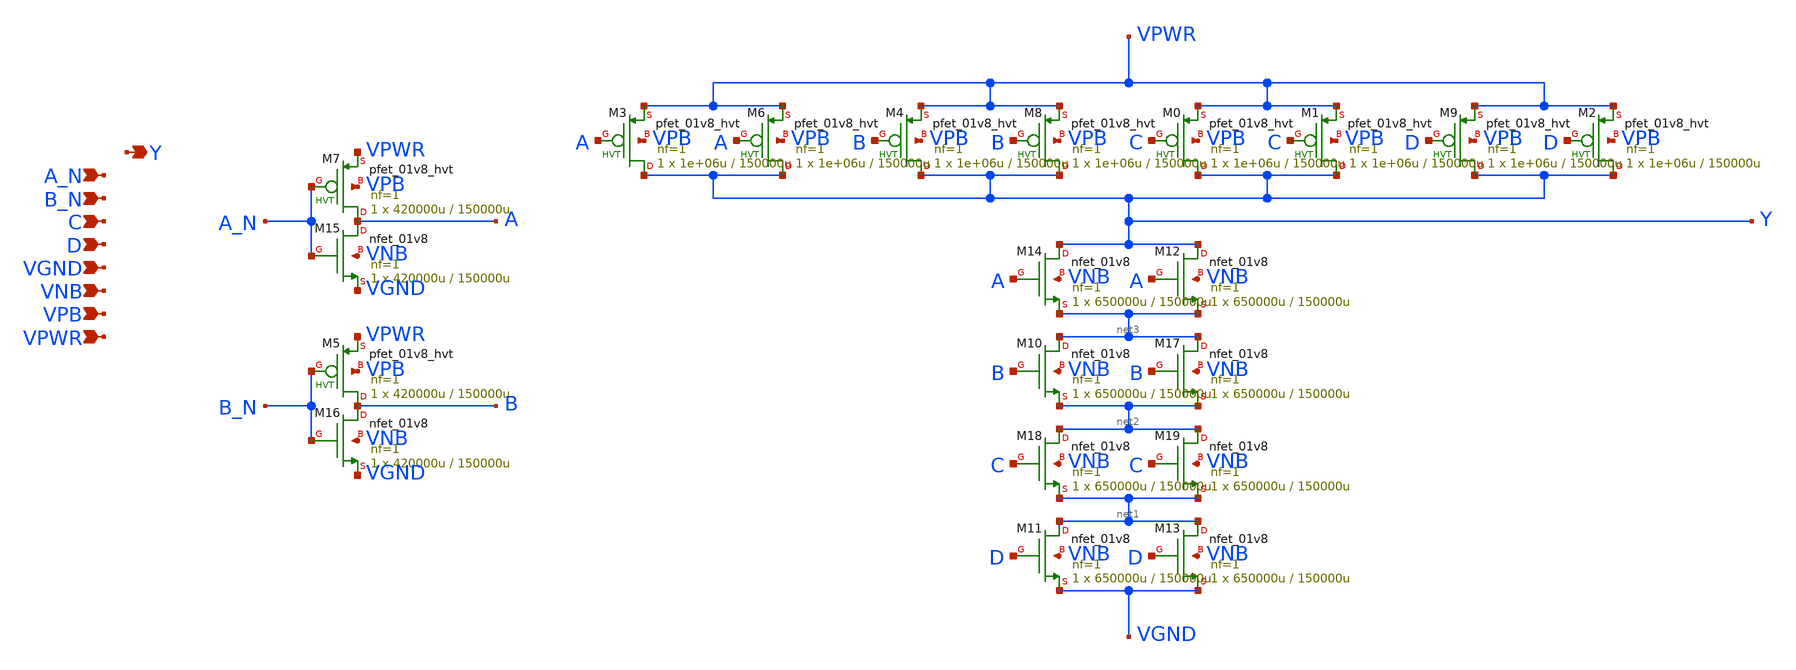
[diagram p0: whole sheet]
** sch_path: schematics/nand4bb/sky130_fd_sc_hd__nand4bb_2.sch
**.subckt sky130_fd_sc_hd__nand4bb_2 A_N B_N C D VGND VNB VPB VPWR Y
*.ipin A_N
*.ipin B_N
*.ipin C
*.ipin D
*.ipin VGND
*.ipin VNB
*.ipin VPB
*.ipin VPWR
*.opin Y
XM0 Y C VPWR VPB sky130_fd_pr__pfet_01v8_hvt L=150000u W=1e+06u nf=1 ad='int((1 + 1)/2) * 1e+06u / 1 * 0.29'
+ as='int((1 + 2)/2) * 1e+06u / 1 * 0.29' pd='2*int((1 + 1)/2) * (1e+06u / 1 + 0.29)' ps='2*int((1 + 2)/2) * (1e+06u / 1 + 0.29)'
+ nrd='0.29 / 1e+06u ' nrs='0.29 / 1e+06u ' sa=0 sb=0 sd=0 mult=1 m=1
XM1 Y C VPWR VPB sky130_fd_pr__pfet_01v8_hvt L=150000u W=1e+06u nf=1 ad='int((1 + 1)/2) * 1e+06u / 1 * 0.29'
+ as='int((1 + 2)/2) * 1e+06u / 1 * 0.29' pd='2*int((1 + 1)/2) * (1e+06u / 1 + 0.29)' ps='2*int((1 + 2)/2) * (1e+06u / 1 + 0.29)'
+ nrd='0.29 / 1e+06u ' nrs='0.29 / 1e+06u ' sa=0 sb=0 sd=0 mult=1 m=1
XM2 Y D VPWR VPB sky130_fd_pr__pfet_01v8_hvt L=150000u W=1e+06u nf=1 ad='int((1 + 1)/2) * 1e+06u / 1 * 0.29'
+ as='int((1 + 2)/2) * 1e+06u / 1 * 0.29' pd='2*int((1 + 1)/2) * (1e+06u / 1 + 0.29)' ps='2*int((1 + 2)/2) * (1e+06u / 1 + 0.29)'
+ nrd='0.29 / 1e+06u ' nrs='0.29 / 1e+06u ' sa=0 sb=0 sd=0 mult=1 m=1
XM3 Y A VPWR VPB sky130_fd_pr__pfet_01v8_hvt L=150000u W=1e+06u nf=1 ad='int((1 + 1)/2) * 1e+06u / 1 * 0.29'
+ as='int((1 + 2)/2) * 1e+06u / 1 * 0.29' pd='2*int((1 + 1)/2) * (1e+06u / 1 + 0.29)' ps='2*int((1 + 2)/2) * (1e+06u / 1 + 0.29)'
+ nrd='0.29 / 1e+06u ' nrs='0.29 / 1e+06u ' sa=0 sb=0 sd=0 mult=1 m=1
XM4 Y B VPWR VPB sky130_fd_pr__pfet_01v8_hvt L=150000u W=1e+06u nf=1 ad='int((1 + 1)/2) * 1e+06u / 1 * 0.29'
+ as='int((1 + 2)/2) * 1e+06u / 1 * 0.29' pd='2*int((1 + 1)/2) * (1e+06u / 1 + 0.29)' ps='2*int((1 + 2)/2) * (1e+06u / 1 + 0.29)'
+ nrd='0.29 / 1e+06u ' nrs='0.29 / 1e+06u ' sa=0 sb=0 sd=0 mult=1 m=1
XM5 B B_N VPWR VPB sky130_fd_pr__pfet_01v8_hvt L=150000u W=420000u nf=1 ad='int((1 + 1)/2) * 420000u / 1 * 0.29'
+ as='int((1 + 2)/2) * 420000u / 1 * 0.29' pd='2*int((1 + 1)/2) * (420000u / 1 + 0.29)' ps='2*int((1 + 2)/2) * (420000u / 1 + 0.29)'
+ nrd='0.29 / 420000u ' nrs='0.29 / 420000u ' sa=0 sb=0 sd=0 mult=1 m=1
XM6 Y A VPWR VPB sky130_fd_pr__pfet_01v8_hvt L=150000u W=1e+06u nf=1 ad='int((1 + 1)/2) * 1e+06u / 1 * 0.29'
+ as='int((1 + 2)/2) * 1e+06u / 1 * 0.29' pd='2*int((1 + 1)/2) * (1e+06u / 1 + 0.29)' ps='2*int((1 + 2)/2) * (1e+06u / 1 + 0.29)'
+ nrd='0.29 / 1e+06u ' nrs='0.29 / 1e+06u ' sa=0 sb=0 sd=0 mult=1 m=1
XM7 A A_N VPWR VPB sky130_fd_pr__pfet_01v8_hvt L=150000u W=420000u nf=1 ad='int((1 + 1)/2) * 420000u / 1 * 0.29'
+ as='int((1 + 2)/2) * 420000u / 1 * 0.29' pd='2*int((1 + 1)/2) * (420000u / 1 + 0.29)' ps='2*int((1 + 2)/2) * (420000u / 1 + 0.29)'
+ nrd='0.29 / 420000u ' nrs='0.29 / 420000u ' sa=0 sb=0 sd=0 mult=1 m=1
XM8 Y B VPWR VPB sky130_fd_pr__pfet_01v8_hvt L=150000u W=1e+06u nf=1 ad='int((1 + 1)/2) * 1e+06u / 1 * 0.29'
+ as='int((1 + 2)/2) * 1e+06u / 1 * 0.29' pd='2*int((1 + 1)/2) * (1e+06u / 1 + 0.29)' ps='2*int((1 + 2)/2) * (1e+06u / 1 + 0.29)'
+ nrd='0.29 / 1e+06u ' nrs='0.29 / 1e+06u ' sa=0 sb=0 sd=0 mult=1 m=1
XM9 Y D VPWR VPB sky130_fd_pr__pfet_01v8_hvt L=150000u W=1e+06u nf=1 ad='int((1 + 1)/2) * 1e+06u / 1 * 0.29'
+ as='int((1 + 2)/2) * 1e+06u / 1 * 0.29' pd='2*int((1 + 1)/2) * (1e+06u / 1 + 0.29)' ps='2*int((1 + 2)/2) * (1e+06u / 1 + 0.29)'
+ nrd='0.29 / 1e+06u ' nrs='0.29 / 1e+06u ' sa=0 sb=0 sd=0 mult=1 m=1
XM10 net3 B net2 VNB sky130_fd_pr__nfet_01v8 L=150000u W=650000u nf=1 ad='int((1 + 1)/2) * 650000u / 1 * 0.29'
+ as='int((1 + 2)/2) * 650000u / 1 * 0.29' pd='2*int((1 + 1)/2) * (650000u / 1 + 0.29)' ps='2*int((1 + 2)/2) * (650000u / 1 + 0.29)'
+ nrd='0.29 / 650000u ' nrs='0.29 / 650000u ' sa=0 sb=0 sd=0 mult=1 m=1
XM11 net1 D VGND VNB sky130_fd_pr__nfet_01v8 L=150000u W=650000u nf=1 ad='int((1 + 1)/2) * 650000u / 1 * 0.29'
+ as='int((1 + 2)/2) * 650000u / 1 * 0.29' pd='2*int((1 + 1)/2) * (650000u / 1 + 0.29)' ps='2*int((1 + 2)/2) * (650000u / 1 + 0.29)'
+ nrd='0.29 / 650000u ' nrs='0.29 / 650000u ' sa=0 sb=0 sd=0 mult=1 m=1
XM12 Y A net3 VNB sky130_fd_pr__nfet_01v8 L=150000u W=650000u nf=1 ad='int((1 + 1)/2) * 650000u / 1 * 0.29'
+ as='int((1 + 2)/2) * 650000u / 1 * 0.29' pd='2*int((1 + 1)/2) * (650000u / 1 + 0.29)' ps='2*int((1 + 2)/2) * (650000u / 1 + 0.29)'
+ nrd='0.29 / 650000u ' nrs='0.29 / 650000u ' sa=0 sb=0 sd=0 mult=1 m=1
XM13 net1 D VGND VNB sky130_fd_pr__nfet_01v8 L=150000u W=650000u nf=1 ad='int((1 + 1)/2) * 650000u / 1 * 0.29'
+ as='int((1 + 2)/2) * 650000u / 1 * 0.29' pd='2*int((1 + 1)/2) * (650000u / 1 + 0.29)' ps='2*int((1 + 2)/2) * (650000u / 1 + 0.29)'
+ nrd='0.29 / 650000u ' nrs='0.29 / 650000u ' sa=0 sb=0 sd=0 mult=1 m=1
XM14 Y A net3 VNB sky130_fd_pr__nfet_01v8 L=150000u W=650000u nf=1 ad='int((1 + 1)/2) * 650000u / 1 * 0.29'
+ as='int((1 + 2)/2) * 650000u / 1 * 0.29' pd='2*int((1 + 1)/2) * (650000u / 1 + 0.29)' ps='2*int((1 + 2)/2) * (650000u / 1 + 0.29)'
+ nrd='0.29 / 650000u ' nrs='0.29 / 650000u ' sa=0 sb=0 sd=0 mult=1 m=1
XM15 A A_N VGND VNB sky130_fd_pr__nfet_01v8 L=150000u W=420000u nf=1 ad='int((1 + 1)/2) * 420000u / 1 * 0.29'
+ as='int((1 + 2)/2) * 420000u / 1 * 0.29' pd='2*int((1 + 1)/2) * (420000u / 1 + 0.29)' ps='2*int((1 + 2)/2) * (420000u / 1 + 0.29)'
+ nrd='0.29 / 420000u ' nrs='0.29 / 420000u ' sa=0 sb=0 sd=0 mult=1 m=1
XM16 B B_N VGND VNB sky130_fd_pr__nfet_01v8 L=150000u W=420000u nf=1 ad='int((1 + 1)/2) * 420000u / 1 * 0.29'
+ as='int((1 + 2)/2) * 420000u / 1 * 0.29' pd='2*int((1 + 1)/2) * (420000u / 1 + 0.29)' ps='2*int((1 + 2)/2) * (420000u / 1 + 0.29)'
+ nrd='0.29 / 420000u ' nrs='0.29 / 420000u ' sa=0 sb=0 sd=0 mult=1 m=1
XM17 net3 B net2 VNB sky130_fd_pr__nfet_01v8 L=150000u W=650000u nf=1 ad='int((1 + 1)/2) * 650000u / 1 * 0.29'
+ as='int((1 + 2)/2) * 650000u / 1 * 0.29' pd='2*int((1 + 1)/2) * (650000u / 1 + 0.29)' ps='2*int((1 + 2)/2) * (650000u / 1 + 0.29)'
+ nrd='0.29 / 650000u ' nrs='0.29 / 650000u ' sa=0 sb=0 sd=0 mult=1 m=1
XM18 net2 C net1 VNB sky130_fd_pr__nfet_01v8 L=150000u W=650000u nf=1 ad='int((1 + 1)/2) * 650000u / 1 * 0.29'
+ as='int((1 + 2)/2) * 650000u / 1 * 0.29' pd='2*int((1 + 1)/2) * (650000u / 1 + 0.29)' ps='2*int((1 + 2)/2) * (650000u / 1 + 0.29)'
+ nrd='0.29 / 650000u ' nrs='0.29 / 650000u ' sa=0 sb=0 sd=0 mult=1 m=1
XM19 net2 C net1 VNB sky130_fd_pr__nfet_01v8 L=150000u W=650000u nf=1 ad='int((1 + 1)/2) * 650000u / 1 * 0.29'
+ as='int((1 + 2)/2) * 650000u / 1 * 0.29' pd='2*int((1 + 1)/2) * (650000u / 1 + 0.29)' ps='2*int((1 + 2)/2) * (650000u / 1 + 0.29)'
+ nrd='0.29 / 650000u ' nrs='0.29 / 650000u ' sa=0 sb=0 sd=0 mult=1 m=1
**.ends
.end
